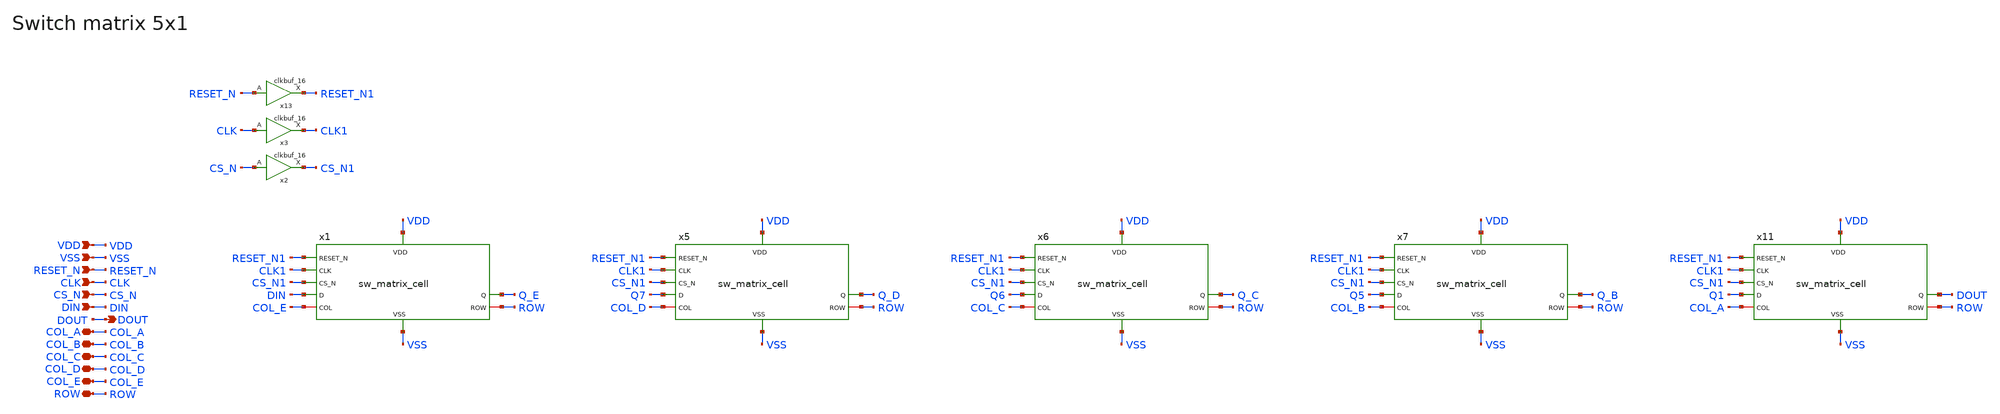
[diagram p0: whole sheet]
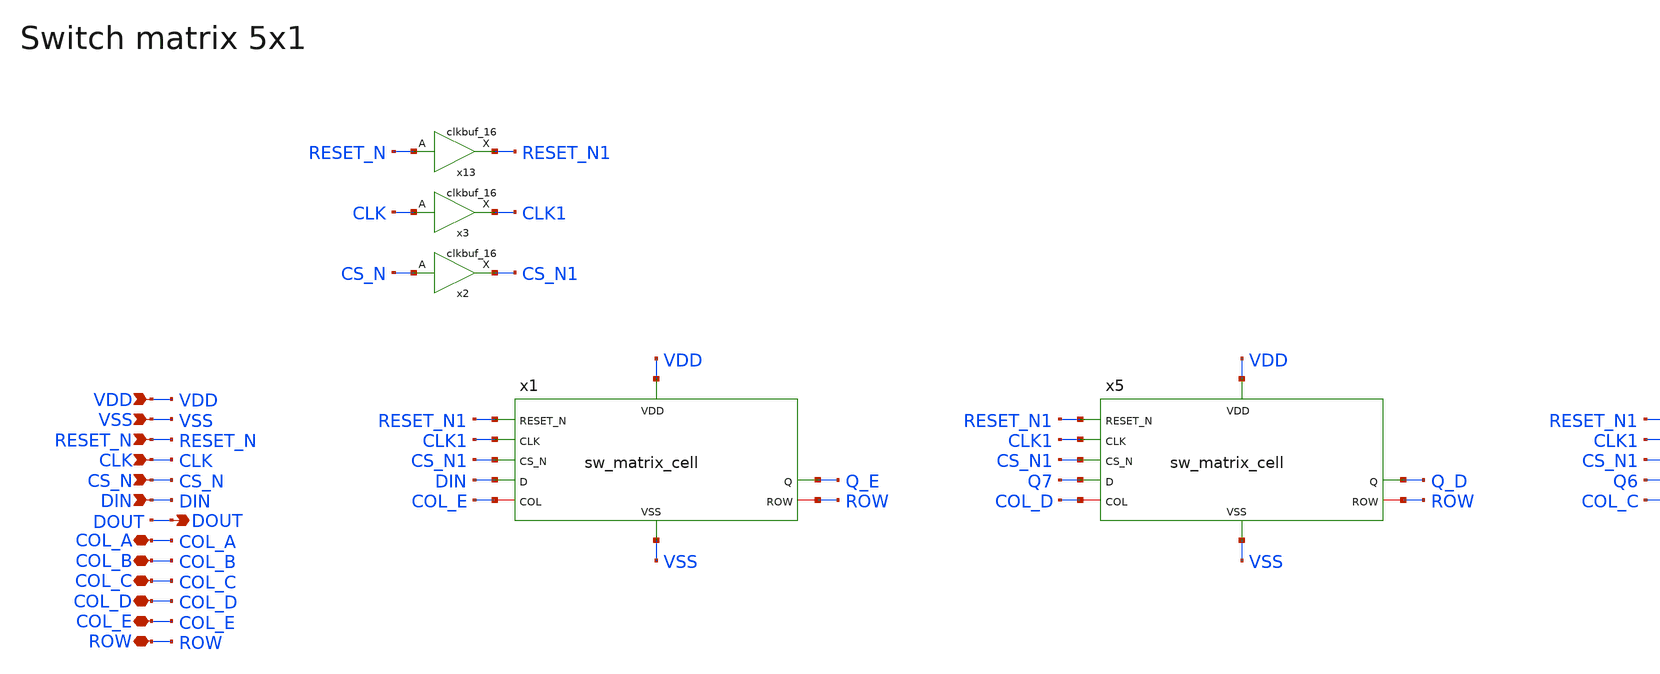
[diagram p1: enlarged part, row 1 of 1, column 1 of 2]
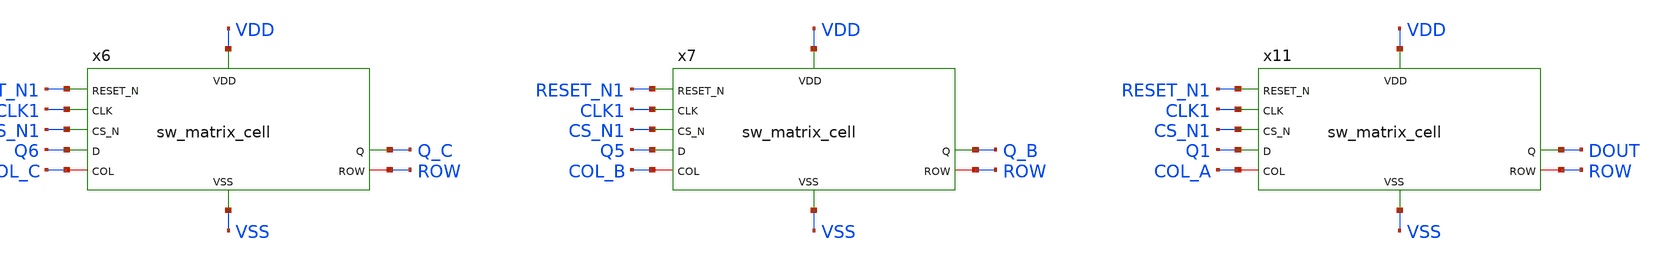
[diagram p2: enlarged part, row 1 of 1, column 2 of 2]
** sch_path: designs/libs/core_analog/sw_matrix/sw_matrix_5x1.sch
* Copyright 2022 GlobalFoundries PDK Authors
* Licensed under the Apache License, Version 2.0 (the "License");
* you may not use this file except in compliance with the License.
* You may obtain a copy of the License at
* https://www.apache.org/licenses/LICENSE-2.0
* Unless required by applicable law or agreed to in writing, software
* distributed under the License is distributed on an "AS IS" BASIS,
* WITHOUT WARRANTIES OR CONDITIONS OF ANY KIND, either express or implied.
* See the License for the specific language governing permissions and
* limitations under the License.
**.subckt sw_matrix_5x1 VDD VSS RESET_N CLK CS_N DIN COL_A COL_B COL_C COL_D ROW DOUT COL_E
*.ipin VDD
*.ipin VSS
*.ipin RESET_N
*.ipin CLK
*.ipin CS_N
*.ipin DIN
*.iopin COL_A
*.iopin COL_B
*.iopin COL_C
*.iopin COL_D
*.iopin ROW
*.opin DOUT
*.iopin COL_E
x1 VDD VSS RESET_N1 CLK1 DIN CS_N1 Q_E COL_E ROW sw_matrix_cell
x5 VDD VSS RESET_N1 CLK1 Q7 CS_N1 Q_D COL_D ROW sw_matrix_cell
x6 VDD VSS RESET_N1 CLK1 Q6 CS_N1 Q_C COL_C ROW sw_matrix_cell
x7 VDD VSS RESET_N1 CLK1 Q5 CS_N1 Q_B COL_B ROW sw_matrix_cell
x11 VDD VSS RESET_N1 CLK1 Q1 CS_N1 DOUT COL_A ROW sw_matrix_cell
x3 CLK CLK1 VDD VDD VSS VSS gf180mcu_fd_sc_mcu7t5v0__clkbuf_16
x13 RESET_N RESET_N1 VDD VDD VSS VSS gf180mcu_fd_sc_mcu7t5v0__clkbuf_16
x2 CS_N CS_N1 VDD VDD VSS VSS gf180mcu_fd_sc_mcu7t5v0__clkbuf_16
**.ends
.end
